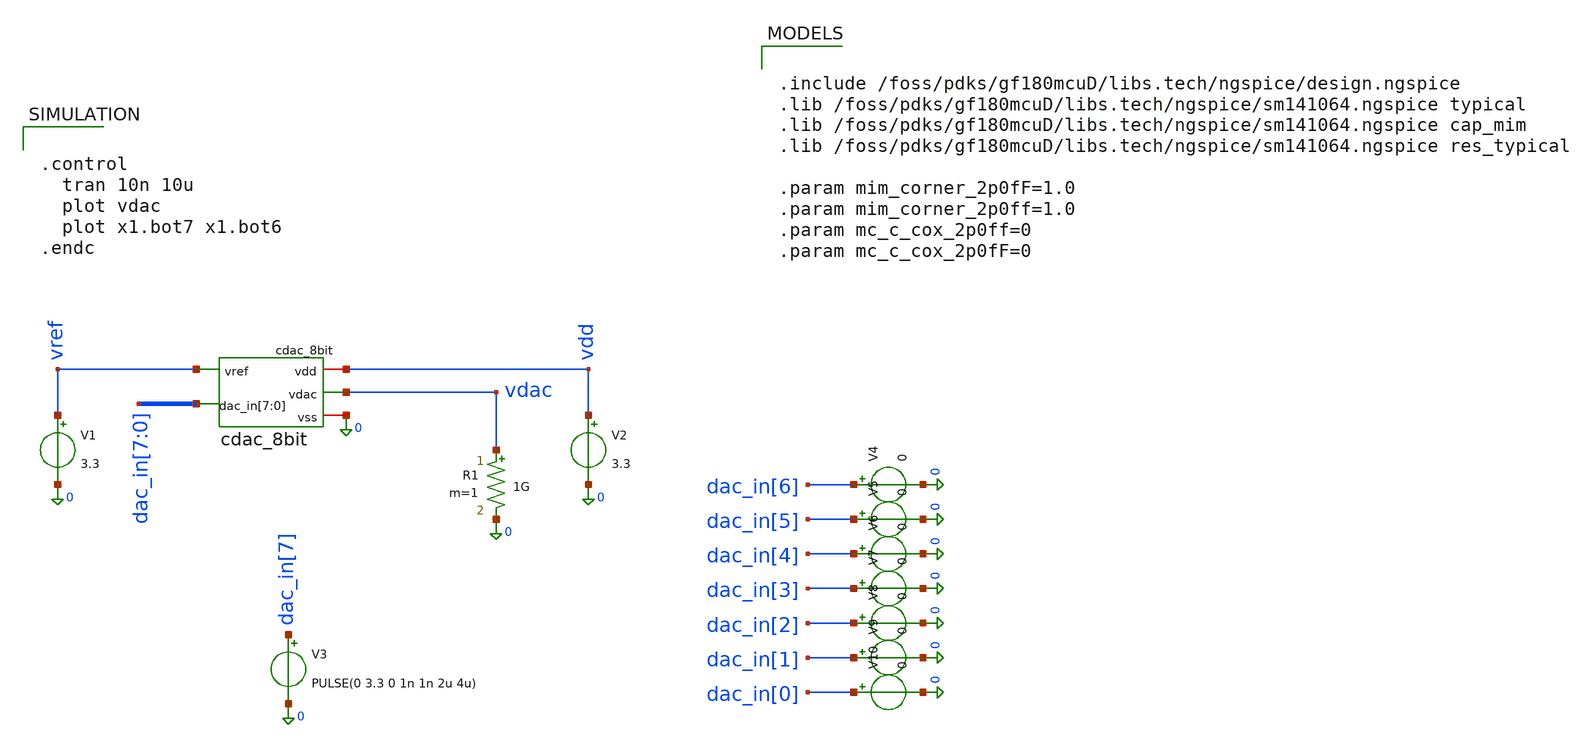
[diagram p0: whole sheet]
** sch_path: xschem/sar_adc/blocks/cdac/testbench/tb_cdac_8bit.sch
**.subckt tb_cdac_8bit
V1 vref 0 3.3
V2 vdd 0 3.3
R1 vdac 0 1G m=1
V3 dac_in[7] 0 PULSE(0 3.3 0 1n 1n 2u 4u)
V4 dac_in[6] 0 0
V5 dac_in[5] 0 0
V6 dac_in[4] 0 0
V7 dac_in[3] 0 0
V8 dac_in[2] 0 0
V9 dac_in[1] 0 0
V10 dac_in[0] 0 0
x1 vref vdd 0 dac_in[7] dac_in[6] dac_in[5] dac_in[4] dac_in[3] dac_in[2] dac_in[1] dac_in[0] vdac
+ cdac_8bit
**** begin user architecture code


.include /foss/pdks/gf180mcuD/libs.tech/ngspice/design.ngspice
.lib /foss/pdks/gf180mcuD/libs.tech/ngspice/sm141064.ngspice typical
.lib /foss/pdks/gf180mcuD/libs.tech/ngspice/sm141064.ngspice cap_mim
.lib /foss/pdks/gf180mcuD/libs.tech/ngspice/sm141064.ngspice res_typical

.param mim_corner_2p0fF=1.0
.param mim_corner_2p0ff=1.0
.param mc_c_cox_2p0ff=0
.param mc_c_cox_2p0fF=0




.control
  tran 10n 10u
  plot vdac
  plot x1.bot7 x1.bot6
.endc


**** end user architecture code
**.ends
.end
